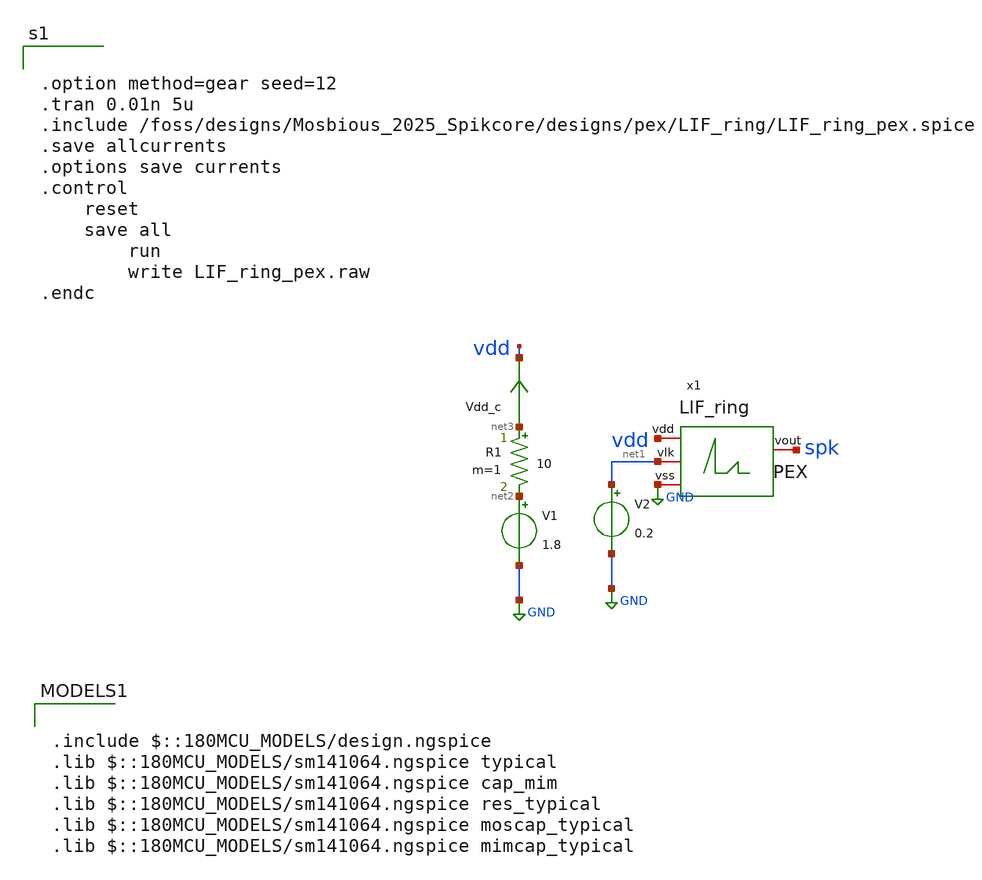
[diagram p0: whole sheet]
** sch_path: designs/pex/LIF_ring/LIF_ring.sch
**.subckt LIF_ring
V1 net2 GND 1.8
Vdd_c net3 vdd 0
.save i(vdd_c)
R1 net3 net2 10 m=1
V2 net1 GND 0.2
x1 vdd net1 spk GND LIF_ring
**** begin user architecture code


.option method=gear seed=12
.tran 0.01n 5u
.include /foss/designs/Mosbious_2025_Spikcore/designs/pex/LIF_ring/LIF_ring_pex.spice
.save allcurrents
.options save currents
.control
	reset
	save all
        run
        write LIF_ring_pex.raw
.endc



.include $::180MCU_MODELS/design.ngspice
.lib $::180MCU_MODELS/sm141064.ngspice typical
.lib $::180MCU_MODELS/sm141064.ngspice cap_mim
.lib $::180MCU_MODELS/sm141064.ngspice res_typical
.lib $::180MCU_MODELS/sm141064.ngspice moscap_typical
.lib $::180MCU_MODELS/sm141064.ngspice mimcap_typical

**** end user architecture code
**.ends
.GLOBAL GND
.end
